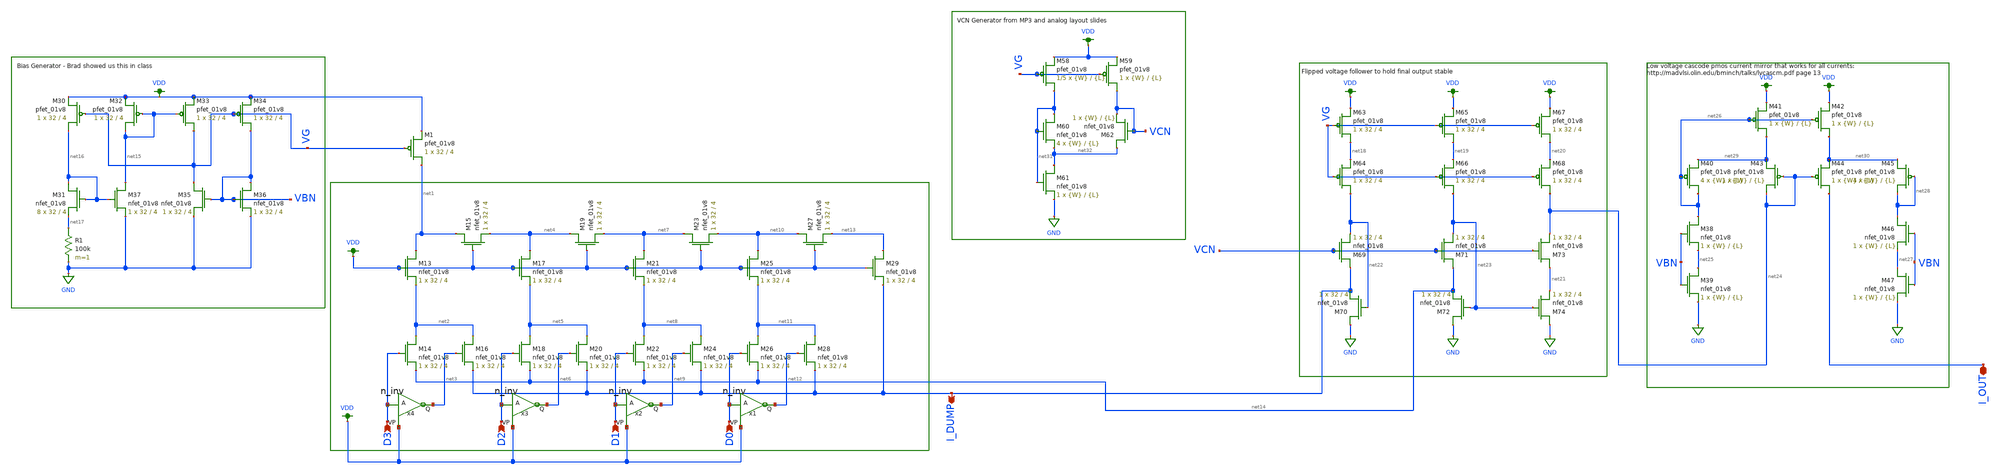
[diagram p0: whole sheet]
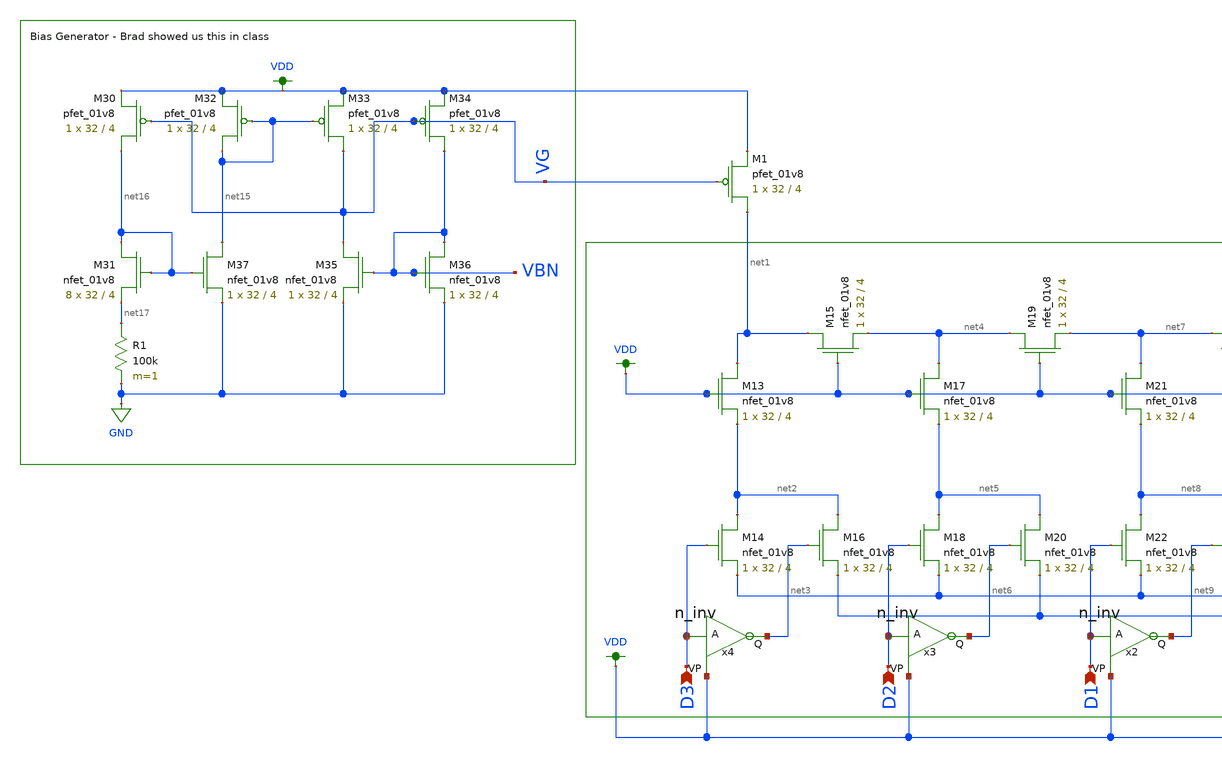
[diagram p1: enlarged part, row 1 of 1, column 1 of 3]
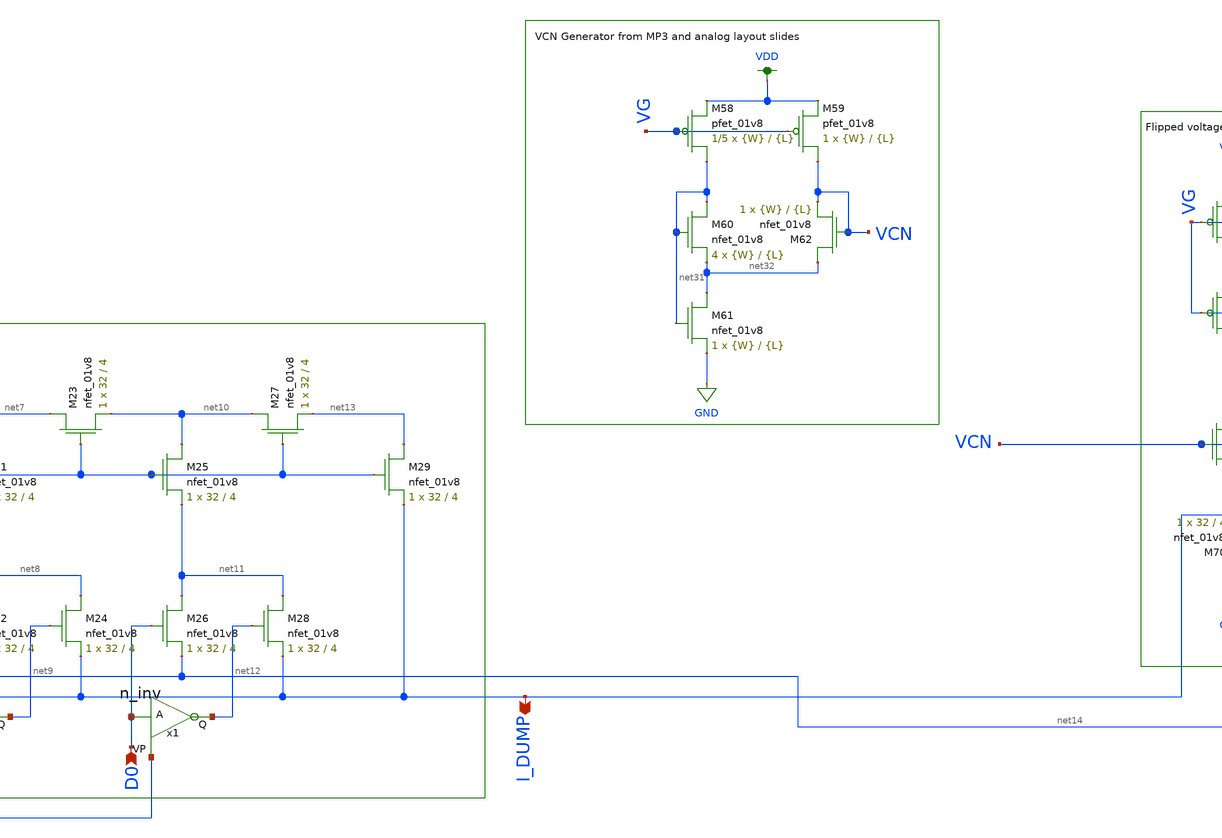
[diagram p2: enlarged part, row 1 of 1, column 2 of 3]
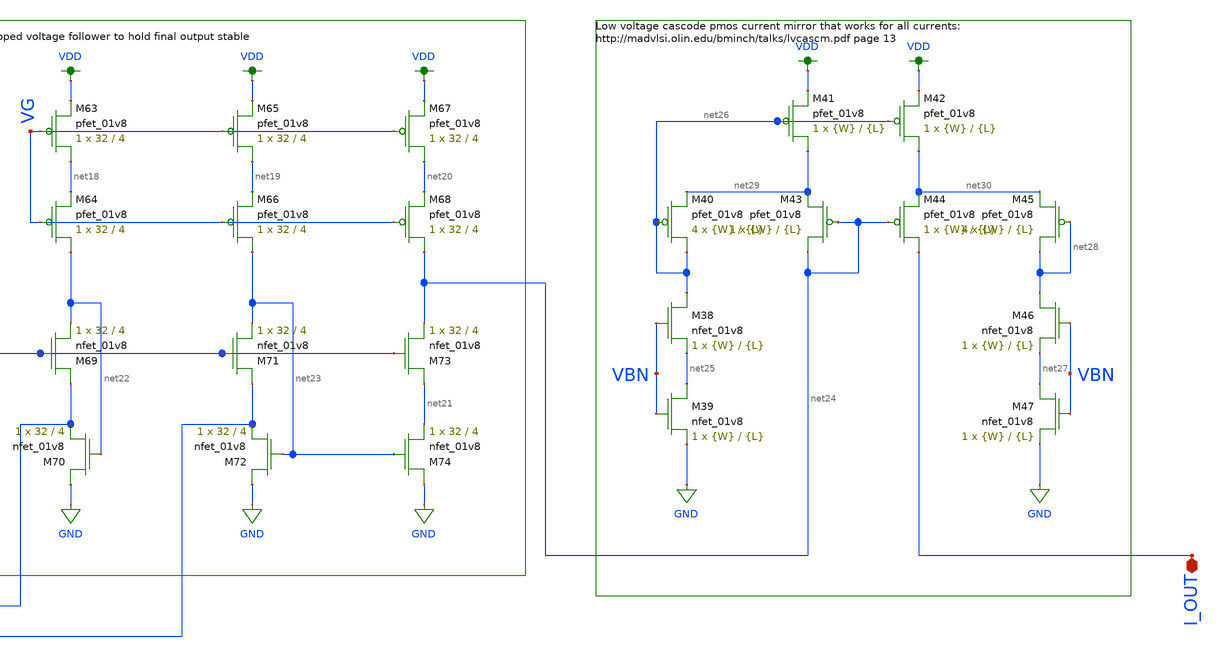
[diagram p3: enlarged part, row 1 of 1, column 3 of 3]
** sch_path: schemas/4BIT_DAC.sch
**.subckt 4BIT_DAC D3 D2 D1 D0 I_DUMP I_OUT
*.ipin D3
*.ipin D2
*.ipin D1
*.ipin D0
*.opin I_DUMP
*.iopin I_OUT
XM13 net1 VDD net2 GND sky130_fd_pr__nfet_01v8 L=4 W=32 nf=1 ad='int((nf+1)/2) * W/nf * 0.29' as='int((nf+2)/2) * W/nf * 0.29'
+ pd='2*int((nf+1)/2) * (W/nf + 0.29)' ps='2*int((nf+2)/2) * (W/nf + 0.29)' nrd='0.29 / W' nrs='0.29 / W'
+ sa=0 sb=0 sd=0 mult=1 m=1
XM14 net2 D3 net14 GND sky130_fd_pr__nfet_01v8 L=4 W=32 nf=1 ad='int((nf+1)/2) * W/nf * 0.29' as='int((nf+2)/2) * W/nf * 0.29'
+ pd='2*int((nf+1)/2) * (W/nf + 0.29)' ps='2*int((nf+2)/2) * (W/nf + 0.29)' nrd='0.29 / W' nrs='0.29 / W'
+ sa=0 sb=0 sd=0 mult=1 m=1
XM15 net1 VDD net4 GND sky130_fd_pr__nfet_01v8 L=4 W=32 nf=1 ad='int((nf+1)/2) * W/nf * 0.29' as='int((nf+2)/2) * W/nf * 0.29'
+ pd='2*int((nf+1)/2) * (W/nf + 0.29)' ps='2*int((nf+2)/2) * (W/nf + 0.29)' nrd='0.29 / W' nrs='0.29 / W'
+ sa=0 sb=0 sd=0 mult=1 m=1
XM16 net2 net3 I_DUMP GND sky130_fd_pr__nfet_01v8 L=4 W=32 nf=1 ad='int((nf+1)/2) * W/nf * 0.29' as='int((nf+2)/2) * W/nf * 0.29'
+ pd='2*int((nf+1)/2) * (W/nf + 0.29)' ps='2*int((nf+2)/2) * (W/nf + 0.29)' nrd='0.29 / W' nrs='0.29 / W'
+ sa=0 sb=0 sd=0 mult=1 m=1
XM17 net4 VDD net5 GND sky130_fd_pr__nfet_01v8 L=4 W=32 nf=1 ad='int((nf+1)/2) * W/nf * 0.29' as='int((nf+2)/2) * W/nf * 0.29'
+ pd='2*int((nf+1)/2) * (W/nf + 0.29)' ps='2*int((nf+2)/2) * (W/nf + 0.29)' nrd='0.29 / W' nrs='0.29 / W'
+ sa=0 sb=0 sd=0 mult=1 m=1
XM18 net5 D2 net14 GND sky130_fd_pr__nfet_01v8 L=4 W=32 nf=1 ad='int((nf+1)/2) * W/nf * 0.29' as='int((nf+2)/2) * W/nf * 0.29'
+ pd='2*int((nf+1)/2) * (W/nf + 0.29)' ps='2*int((nf+2)/2) * (W/nf + 0.29)' nrd='0.29 / W' nrs='0.29 / W'
+ sa=0 sb=0 sd=0 mult=1 m=1
XM19 net4 VDD net7 GND sky130_fd_pr__nfet_01v8 L=4 W=32 nf=1 ad='int((nf+1)/2) * W/nf * 0.29' as='int((nf+2)/2) * W/nf * 0.29'
+ pd='2*int((nf+1)/2) * (W/nf + 0.29)' ps='2*int((nf+2)/2) * (W/nf + 0.29)' nrd='0.29 / W' nrs='0.29 / W'
+ sa=0 sb=0 sd=0 mult=1 m=1
XM20 net5 net6 I_DUMP GND sky130_fd_pr__nfet_01v8 L=4 W=32 nf=1 ad='int((nf+1)/2) * W/nf * 0.29' as='int((nf+2)/2) * W/nf * 0.29'
+ pd='2*int((nf+1)/2) * (W/nf + 0.29)' ps='2*int((nf+2)/2) * (W/nf + 0.29)' nrd='0.29 / W' nrs='0.29 / W'
+ sa=0 sb=0 sd=0 mult=1 m=1
XM21 net7 VDD net8 GND sky130_fd_pr__nfet_01v8 L=4 W=32 nf=1 ad='int((nf+1)/2) * W/nf * 0.29' as='int((nf+2)/2) * W/nf * 0.29'
+ pd='2*int((nf+1)/2) * (W/nf + 0.29)' ps='2*int((nf+2)/2) * (W/nf + 0.29)' nrd='0.29 / W' nrs='0.29 / W'
+ sa=0 sb=0 sd=0 mult=1 m=1
XM22 net8 D1 net14 GND sky130_fd_pr__nfet_01v8 L=4 W=32 nf=1 ad='int((nf+1)/2) * W/nf * 0.29' as='int((nf+2)/2) * W/nf * 0.29'
+ pd='2*int((nf+1)/2) * (W/nf + 0.29)' ps='2*int((nf+2)/2) * (W/nf + 0.29)' nrd='0.29 / W' nrs='0.29 / W'
+ sa=0 sb=0 sd=0 mult=1 m=1
XM23 net7 VDD net10 GND sky130_fd_pr__nfet_01v8 L=4 W=32 nf=1 ad='int((nf+1)/2) * W/nf * 0.29' as='int((nf+2)/2) * W/nf * 0.29'
+ pd='2*int((nf+1)/2) * (W/nf + 0.29)' ps='2*int((nf+2)/2) * (W/nf + 0.29)' nrd='0.29 / W' nrs='0.29 / W'
+ sa=0 sb=0 sd=0 mult=1 m=1
XM24 net8 net9 I_DUMP GND sky130_fd_pr__nfet_01v8 L=4 W=32 nf=1 ad='int((nf+1)/2) * W/nf * 0.29' as='int((nf+2)/2) * W/nf * 0.29'
+ pd='2*int((nf+1)/2) * (W/nf + 0.29)' ps='2*int((nf+2)/2) * (W/nf + 0.29)' nrd='0.29 / W' nrs='0.29 / W'
+ sa=0 sb=0 sd=0 mult=1 m=1
XM25 net10 VDD net11 GND sky130_fd_pr__nfet_01v8 L=4 W=32 nf=1 ad='int((nf+1)/2) * W/nf * 0.29' as='int((nf+2)/2) * W/nf * 0.29'
+ pd='2*int((nf+1)/2) * (W/nf + 0.29)' ps='2*int((nf+2)/2) * (W/nf + 0.29)' nrd='0.29 / W' nrs='0.29 / W'
+ sa=0 sb=0 sd=0 mult=1 m=1
XM26 net11 D0 net14 GND sky130_fd_pr__nfet_01v8 L=4 W=32 nf=1 ad='int((nf+1)/2) * W/nf * 0.29' as='int((nf+2)/2) * W/nf * 0.29'
+ pd='2*int((nf+1)/2) * (W/nf + 0.29)' ps='2*int((nf+2)/2) * (W/nf + 0.29)' nrd='0.29 / W' nrs='0.29 / W'
+ sa=0 sb=0 sd=0 mult=1 m=1
XM27 net10 VDD net13 GND sky130_fd_pr__nfet_01v8 L=4 W=32 nf=1 ad='int((nf+1)/2) * W/nf * 0.29' as='int((nf+2)/2) * W/nf * 0.29'
+ pd='2*int((nf+1)/2) * (W/nf + 0.29)' ps='2*int((nf+2)/2) * (W/nf + 0.29)' nrd='0.29 / W' nrs='0.29 / W'
+ sa=0 sb=0 sd=0 mult=1 m=1
XM28 net11 net12 I_DUMP GND sky130_fd_pr__nfet_01v8 L=4 W=32 nf=1 ad='int((nf+1)/2) * W/nf * 0.29' as='int((nf+2)/2) * W/nf * 0.29'
+ pd='2*int((nf+1)/2) * (W/nf + 0.29)' ps='2*int((nf+2)/2) * (W/nf + 0.29)' nrd='0.29 / W' nrs='0.29 / W'
+ sa=0 sb=0 sd=0 mult=1 m=1
XM29 net13 VDD I_DUMP GND sky130_fd_pr__nfet_01v8 L=4 W=32 nf=1 ad='int((nf+1)/2) * W/nf * 0.29' as='int((nf+2)/2) * W/nf * 0.29'
+ pd='2*int((nf+1)/2) * (W/nf + 0.29)' ps='2*int((nf+2)/2) * (W/nf + 0.29)' nrd='0.29 / W' nrs='0.29 / W'
+ sa=0 sb=0 sd=0 mult=1 m=1
XM30 net16 VG VDD VDD sky130_fd_pr__pfet_01v8 L=4 W=32 nf=1 ad='int((nf+1)/2) * W/nf * 0.29' as='int((nf+2)/2) * W/nf * 0.29'
+ pd='2*int((nf+1)/2) * (W/nf + 0.29)' ps='2*int((nf+2)/2) * (W/nf + 0.29)' nrd='0.29 / W' nrs='0.29 / W'
+ sa=0 sb=0 sd=0 mult=1 m=1
XM31 net16 net16 net17 GND sky130_fd_pr__nfet_01v8 L=4 W=32 nf=1 ad='int((nf+1)/2) * W/nf * 0.29' as='int((nf+2)/2) * W/nf * 0.29'
+ pd='2*int((nf+1)/2) * (W/nf + 0.29)' ps='2*int((nf+2)/2) * (W/nf + 0.29)' nrd='0.29 / W' nrs='0.29 / W'
+ sa=0 sb=0 sd=0 mult=8 m=8
XM32 net15 net15 VDD VDD sky130_fd_pr__pfet_01v8 L=4 W=32 nf=1 ad='int((nf+1)/2) * W/nf * 0.29' as='int((nf+2)/2) * W/nf * 0.29'
+ pd='2*int((nf+1)/2) * (W/nf + 0.29)' ps='2*int((nf+2)/2) * (W/nf + 0.29)' nrd='0.29 / W' nrs='0.29 / W'
+ sa=0 sb=0 sd=0 mult=1 m=1
XM33 VG net15 VDD VDD sky130_fd_pr__pfet_01v8 L=4 W=32 nf=1 ad='int((nf+1)/2) * W/nf * 0.29' as='int((nf+2)/2) * W/nf * 0.29'
+ pd='2*int((nf+1)/2) * (W/nf + 0.29)' ps='2*int((nf+2)/2) * (W/nf + 0.29)' nrd='0.29 / W' nrs='0.29 / W'
+ sa=0 sb=0 sd=0 mult=1 m=1
XM34 VBN VG VDD VDD sky130_fd_pr__pfet_01v8 L=4 W=32 nf=1 ad='int((nf+1)/2) * W/nf * 0.29' as='int((nf+2)/2) * W/nf * 0.29'
+ pd='2*int((nf+1)/2) * (W/nf + 0.29)' ps='2*int((nf+2)/2) * (W/nf + 0.29)' nrd='0.29 / W' nrs='0.29 / W'
+ sa=0 sb=0 sd=0 mult=1 m=1
XM35 VG VBN GND GND sky130_fd_pr__nfet_01v8 L=4 W=32 nf=1 ad='int((nf+1)/2) * W/nf * 0.29' as='int((nf+2)/2) * W/nf * 0.29'
+ pd='2*int((nf+1)/2) * (W/nf + 0.29)' ps='2*int((nf+2)/2) * (W/nf + 0.29)' nrd='0.29 / W' nrs='0.29 / W'
+ sa=0 sb=0 sd=0 mult=1 m=1
XM36 VBN VBN GND GND sky130_fd_pr__nfet_01v8 L=4 W=32 nf=1 ad='int((nf+1)/2) * W/nf * 0.29' as='int((nf+2)/2) * W/nf * 0.29'
+ pd='2*int((nf+1)/2) * (W/nf + 0.29)' ps='2*int((nf+2)/2) * (W/nf + 0.29)' nrd='0.29 / W' nrs='0.29 / W'
+ sa=0 sb=0 sd=0 mult=1 m=1
XM37 net15 net16 GND GND sky130_fd_pr__nfet_01v8 L=4 W=32 nf=1 ad='int((nf+1)/2) * W/nf * 0.29' as='int((nf+2)/2) * W/nf * 0.29'
+ pd='2*int((nf+1)/2) * (W/nf + 0.29)' ps='2*int((nf+2)/2) * (W/nf + 0.29)' nrd='0.29 / W' nrs='0.29 / W'
+ sa=0 sb=0 sd=0 mult=1 m=1
R1 net17 GND 100k m=1
XM63 net18 VG VDD VDD sky130_fd_pr__pfet_01v8 L=4 W=32 nf=1 ad='int((nf+1)/2) * W/nf * 0.29' as='int((nf+2)/2) * W/nf * 0.29'
+ pd='2*int((nf+1)/2) * (W/nf + 0.29)' ps='2*int((nf+2)/2) * (W/nf + 0.29)' nrd='0.29 / W' nrs='0.29 / W'
+ sa=0 sb=0 sd=0 mult=1 m=1
XM64 net22 VG net18 VDD sky130_fd_pr__pfet_01v8 L=4 W=32 nf=1 ad='int((nf+1)/2) * W/nf * 0.29' as='int((nf+2)/2) * W/nf * 0.29'
+ pd='2*int((nf+1)/2) * (W/nf + 0.29)' ps='2*int((nf+2)/2) * (W/nf + 0.29)' nrd='0.29 / W' nrs='0.29 / W'
+ sa=0 sb=0 sd=0 mult=1 m=1
XM65 net19 VG VDD VDD sky130_fd_pr__pfet_01v8 L=4 W=32 nf=1 ad='int((nf+1)/2) * W/nf * 0.29' as='int((nf+2)/2) * W/nf * 0.29'
+ pd='2*int((nf+1)/2) * (W/nf + 0.29)' ps='2*int((nf+2)/2) * (W/nf + 0.29)' nrd='0.29 / W' nrs='0.29 / W'
+ sa=0 sb=0 sd=0 mult=1 m=1
XM66 net23 VG net19 VDD sky130_fd_pr__pfet_01v8 L=4 W=32 nf=1 ad='int((nf+1)/2) * W/nf * 0.29' as='int((nf+2)/2) * W/nf * 0.29'
+ pd='2*int((nf+1)/2) * (W/nf + 0.29)' ps='2*int((nf+2)/2) * (W/nf + 0.29)' nrd='0.29 / W' nrs='0.29 / W'
+ sa=0 sb=0 sd=0 mult=1 m=1
XM67 net20 VG VDD VDD sky130_fd_pr__pfet_01v8 L=4 W=32 nf=1 ad='int((nf+1)/2) * W/nf * 0.29' as='int((nf+2)/2) * W/nf * 0.29'
+ pd='2*int((nf+1)/2) * (W/nf + 0.29)' ps='2*int((nf+2)/2) * (W/nf + 0.29)' nrd='0.29 / W' nrs='0.29 / W'
+ sa=0 sb=0 sd=0 mult=1 m=1
XM68 net24 VG net20 VDD sky130_fd_pr__pfet_01v8 L=4 W=32 nf=1 ad='int((nf+1)/2) * W/nf * 0.29' as='int((nf+2)/2) * W/nf * 0.29'
+ pd='2*int((nf+1)/2) * (W/nf + 0.29)' ps='2*int((nf+2)/2) * (W/nf + 0.29)' nrd='0.29 / W' nrs='0.29 / W'
+ sa=0 sb=0 sd=0 mult=1 m=1
XM69 I_DUMP VCN net22 GND sky130_fd_pr__nfet_01v8 L=4 W=32 nf=1 ad='int((nf+1)/2) * W/nf * 0.29' as='int((nf+2)/2) * W/nf * 0.29'
+ pd='2*int((nf+1)/2) * (W/nf + 0.29)' ps='2*int((nf+2)/2) * (W/nf + 0.29)' nrd='0.29 / W' nrs='0.29 / W'
+ sa=0 sb=0 sd=0 mult=1 m=1
XM70 GND net22 I_DUMP GND sky130_fd_pr__nfet_01v8 L=4 W=32 nf=1 ad='int((nf+1)/2) * W/nf * 0.29' as='int((nf+2)/2) * W/nf * 0.29'
+ pd='2*int((nf+1)/2) * (W/nf + 0.29)' ps='2*int((nf+2)/2) * (W/nf + 0.29)' nrd='0.29 / W' nrs='0.29 / W'
+ sa=0 sb=0 sd=0 mult=1 m=1
XM71 net14 VCN net23 GND sky130_fd_pr__nfet_01v8 L=4 W=32 nf=1 ad='int((nf+1)/2) * W/nf * 0.29' as='int((nf+2)/2) * W/nf * 0.29'
+ pd='2*int((nf+1)/2) * (W/nf + 0.29)' ps='2*int((nf+2)/2) * (W/nf + 0.29)' nrd='0.29 / W' nrs='0.29 / W'
+ sa=0 sb=0 sd=0 mult=1 m=1
XM72 GND net23 net14 GND sky130_fd_pr__nfet_01v8 L=4 W=32 nf=1 ad='int((nf+1)/2) * W/nf * 0.29' as='int((nf+2)/2) * W/nf * 0.29'
+ pd='2*int((nf+1)/2) * (W/nf + 0.29)' ps='2*int((nf+2)/2) * (W/nf + 0.29)' nrd='0.29 / W' nrs='0.29 / W'
+ sa=0 sb=0 sd=0 mult=1 m=1
XM73 net21 VCN net24 GND sky130_fd_pr__nfet_01v8 L=4 W=32 nf=1 ad='int((nf+1)/2) * W/nf * 0.29' as='int((nf+2)/2) * W/nf * 0.29'
+ pd='2*int((nf+1)/2) * (W/nf + 0.29)' ps='2*int((nf+2)/2) * (W/nf + 0.29)' nrd='0.29 / W' nrs='0.29 / W'
+ sa=0 sb=0 sd=0 mult=1 m=1
XM74 GND net23 net21 GND sky130_fd_pr__nfet_01v8 L=4 W=32 nf=1 ad='int((nf+1)/2) * W/nf * 0.29' as='int((nf+2)/2) * W/nf * 0.29'
+ pd='2*int((nf+1)/2) * (W/nf + 0.29)' ps='2*int((nf+2)/2) * (W/nf + 0.29)' nrd='0.29 / W' nrs='0.29 / W'
+ sa=0 sb=0 sd=0 mult=1 m=1
XM1 net1 VG VDD VDD sky130_fd_pr__pfet_01v8 L=4 W=32 nf=1 ad='int((nf+1)/2) * W/nf * 0.29' as='int((nf+2)/2) * W/nf * 0.29'
+ pd='2*int((nf+1)/2) * (W/nf + 0.29)' ps='2*int((nf+2)/2) * (W/nf + 0.29)' nrd='0.29 / W' nrs='0.29 / W'
+ sa=0 sb=0 sd=0 mult=1 m=1
x1 VDD net12 D0 n_inv
x2 VDD net9 D1 n_inv
x3 VDD net6 D2 n_inv
x4 VDD net3 D3 n_inv
XM38 net26 VBN net25 GND sky130_fd_pr__nfet_01v8 L={L} W={W} nf=1 ad='int((nf+1)/2) * W/nf * 0.29' as='int((nf+2)/2) * W/nf * 0.29'
+ pd='2*int((nf+1)/2) * (W/nf + 0.29)' ps='2*int((nf+2)/2) * (W/nf + 0.29)' nrd='0.29 / W' nrs='0.29 / W'
+ sa=0 sb=0 sd=0 mult=1 m=1
XM39 net25 VBN GND GND sky130_fd_pr__nfet_01v8 L={L} W={W} nf=1 ad='int((nf+1)/2) * W/nf * 0.29' as='int((nf+2)/2) * W/nf * 0.29'
+ pd='2*int((nf+1)/2) * (W/nf + 0.29)' ps='2*int((nf+2)/2) * (W/nf + 0.29)' nrd='0.29 / W' nrs='0.29 / W'
+ sa=0 sb=0 sd=0 mult=1 m=1
XM40 net26 net26 net29 VDD sky130_fd_pr__pfet_01v8 L={L} W={W} nf=1 ad='int((nf+1)/2) * W/nf * 0.29'
+ as='int((nf+2)/2) * W/nf * 0.29' pd='2*int((nf+1)/2) * (W/nf + 0.29)' ps='2*int((nf+2)/2) * (W/nf + 0.29)'
+ nrd='0.29 / W' nrs='0.29 / W' sa=0 sb=0 sd=0 mult=4 m=4
XM41 net29 net26 VDD VDD sky130_fd_pr__pfet_01v8 L={L} W={W} nf=1 ad='int((nf+1)/2) * W/nf * 0.29' as='int((nf+2)/2) * W/nf * 0.29'
+ pd='2*int((nf+1)/2) * (W/nf + 0.29)' ps='2*int((nf+2)/2) * (W/nf + 0.29)' nrd='0.29 / W' nrs='0.29 / W'
+ sa=0 sb=0 sd=0 mult=1 m=1
XM42 net30 net26 VDD VDD sky130_fd_pr__pfet_01v8 L={L} W={W} nf=1 ad='int((nf+1)/2) * W/nf * 0.29' as='int((nf+2)/2) * W/nf * 0.29'
+ pd='2*int((nf+1)/2) * (W/nf + 0.29)' ps='2*int((nf+2)/2) * (W/nf + 0.29)' nrd='0.29 / W' nrs='0.29 / W'
+ sa=0 sb=0 sd=0 mult=1 m=1
XM43 net24 net24 net29 VDD sky130_fd_pr__pfet_01v8 L={L} W={W} nf=1 ad='int((nf+1)/2) * W/nf * 0.29'
+ as='int((nf+2)/2) * W/nf * 0.29' pd='2*int((nf+1)/2) * (W/nf + 0.29)' ps='2*int((nf+2)/2) * (W/nf + 0.29)'
+ nrd='0.29 / W' nrs='0.29 / W' sa=0 sb=0 sd=0 mult=1 m=1
XM44 I_OUT net24 net30 VDD sky130_fd_pr__pfet_01v8 L={L} W={W} nf=1 ad='int((nf+1)/2) * W/nf * 0.29'
+ as='int((nf+2)/2) * W/nf * 0.29' pd='2*int((nf+1)/2) * (W/nf + 0.29)' ps='2*int((nf+2)/2) * (W/nf + 0.29)'
+ nrd='0.29 / W' nrs='0.29 / W' sa=0 sb=0 sd=0 mult=1 m=1
XM45 net28 net28 net30 VDD sky130_fd_pr__pfet_01v8 L={L} W={W} nf=1 ad='int((nf+1)/2) * W/nf * 0.29'
+ as='int((nf+2)/2) * W/nf * 0.29' pd='2*int((nf+1)/2) * (W/nf + 0.29)' ps='2*int((nf+2)/2) * (W/nf + 0.29)'
+ nrd='0.29 / W' nrs='0.29 / W' sa=0 sb=0 sd=0 mult=4 m=4
XM46 net28 VBN net27 GND sky130_fd_pr__nfet_01v8 L={L} W={W} nf=1 ad='int((nf+1)/2) * W/nf * 0.29' as='int((nf+2)/2) * W/nf * 0.29'
+ pd='2*int((nf+1)/2) * (W/nf + 0.29)' ps='2*int((nf+2)/2) * (W/nf + 0.29)' nrd='0.29 / W' nrs='0.29 / W'
+ sa=0 sb=0 sd=0 mult=1 m=1
XM47 net27 VBN GND GND sky130_fd_pr__nfet_01v8 L={L} W={W} nf=1 ad='int((nf+1)/2) * W/nf * 0.29' as='int((nf+2)/2) * W/nf * 0.29'
+ pd='2*int((nf+1)/2) * (W/nf + 0.29)' ps='2*int((nf+2)/2) * (W/nf + 0.29)' nrd='0.29 / W' nrs='0.29 / W'
+ sa=0 sb=0 sd=0 mult=1 m=1
XM58 net31 VG VDD VDD sky130_fd_pr__pfet_01v8 L={L} W={W} nf=1 ad='int((nf+1)/2) * W/nf * 0.29' as='int((nf+2)/2) * W/nf * 0.29'
+ pd='2*int((nf+1)/2) * (W/nf + 0.29)' ps='2*int((nf+2)/2) * (W/nf + 0.29)' nrd='0.29 / W' nrs='0.29 / W'
+ sa=0 sb=0 sd=0 mult=1/5 m=1/5
XM59 VCN VG VDD VDD sky130_fd_pr__pfet_01v8 L={L} W={W} nf=1 ad='int((nf+1)/2) * W/nf * 0.29' as='int((nf+2)/2) * W/nf * 0.29'
+ pd='2*int((nf+1)/2) * (W/nf + 0.29)' ps='2*int((nf+2)/2) * (W/nf + 0.29)' nrd='0.29 / W' nrs='0.29 / W'
+ sa=0 sb=0 sd=0 mult=1 m=1
XM60 net31 net31 net32 GND sky130_fd_pr__nfet_01v8 L={L} W={W} nf=1 ad='int((nf+1)/2) * W/nf * 0.29'
+ as='int((nf+2)/2) * W/nf * 0.29' pd='2*int((nf+1)/2) * (W/nf + 0.29)' ps='2*int((nf+2)/2) * (W/nf + 0.29)'
+ nrd='0.29 / W' nrs='0.29 / W' sa=0 sb=0 sd=0 mult=4 m=4
XM61 net32 net31 GND GND sky130_fd_pr__nfet_01v8 L={L} W={W} nf=1 ad='int((nf+1)/2) * W/nf * 0.29' as='int((nf+2)/2) * W/nf * 0.29'
+ pd='2*int((nf+1)/2) * (W/nf + 0.29)' ps='2*int((nf+2)/2) * (W/nf + 0.29)' nrd='0.29 / W' nrs='0.29 / W'
+ sa=0 sb=0 sd=0 mult=1 m=1
XM62 net32 VCN VCN GND sky130_fd_pr__nfet_01v8 L={L} W={W} nf=1 ad='int((nf+1)/2) * W/nf * 0.29' as='int((nf+2)/2) * W/nf * 0.29'
+ pd='2*int((nf+1)/2) * (W/nf + 0.29)' ps='2*int((nf+2)/2) * (W/nf + 0.29)' nrd='0.29 / W' nrs='0.29 / W'
+ sa=0 sb=0 sd=0 mult=1 m=1
**.ends

* expanding   symbol:  /home/lxbtlr/DTILO/schemas/n_inv.sym # of pins=3
** sym_path: schemas/n_inv.sym
** sch_path: schemas/n_inv.sch
.subckt n_inv VP Q A
*.ipin A
*.ipin VP
*.opin Q
XM1 Q A GND GND sky130_fd_pr__nfet_01v8 L={invL} W={invW} nf=1 ad='int((nf+1)/2) * W/nf * 0.29' as='int((nf+2)/2) * W/nf * 0.29'
+ pd='2*int((nf+1)/2) * (W/nf + 0.29)' ps='2*int((nf+2)/2) * (W/nf + 0.29)' nrd='0.29 / W' nrs='0.29 / W'
+ sa=0 sb=0 sd=0 mult=1 m=1
XM2 Q A VP VDD sky130_fd_pr__pfet_01v8 L={L} W={W} nf=1 ad='int((nf+1)/2) * W/nf * 0.29' as='int((nf+2)/2) * W/nf * 0.29'
+ pd='2*int((nf+1)/2) * (W/nf + 0.29)' ps='2*int((nf+2)/2) * (W/nf + 0.29)' nrd='0.29 / W' nrs='0.29 / W'
+ sa=0 sb=0 sd=0 mult=1 m=1
.ends

.GLOBAL GND
.GLOBAL VDD
.end
